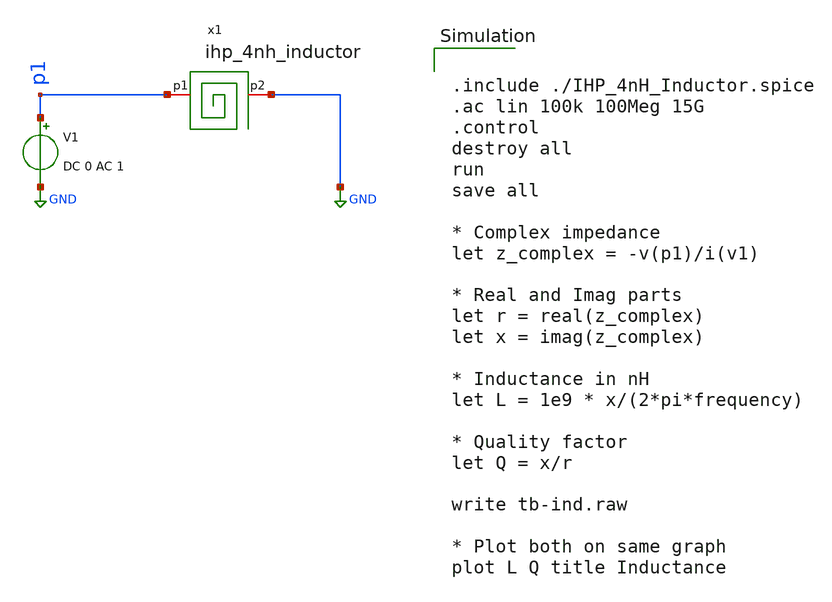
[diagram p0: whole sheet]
** sch_path: xschem/lc-vco/inductor/tb-ind.sch
**.subckt tb-ind
V1 p1 GND DC 0 AC 1
x1 p1 GND ihp_4nh_inductor
**** begin user architecture code


.include ./IHP_4nH_Inductor.spice
.ac lin 100k 100Meg 15G
.control
destroy all
run
save all

* Complex impedance
let z_complex = -v(p1)/i(v1)

* Real and Imag parts
let r = real(z_complex)
let x = imag(z_complex)

* Inductance in nH
let L = 1e9 * x/(2*pi*frequency)

* Quality factor
let Q = x/r

write tb-ind.raw

* Plot both on same graph
plot L Q title Inductance

**** end user architecture code
**.ends
.GLOBAL GND
.end
